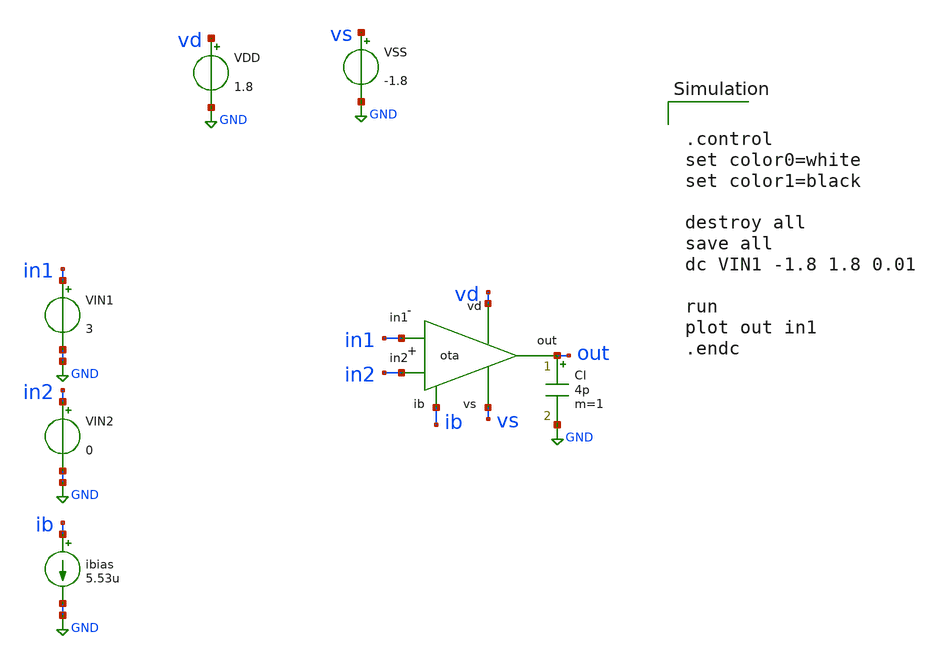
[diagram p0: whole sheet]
** sch_path: amp-op/xschem/ota_tb-dc.sch
* Copyright 2020 Stefan Frederik Schippers
* Licensed under the Apache License, Version 2.0 (the "License");
* you may not use this file except in compliance with the License.
* You may obtain a copy of the License at
* https://www.apache.org/licenses/LICENSE-2.0
* Unless required by applicable law or agreed to in writing, software
* distributed under the License is distributed on an "AS IS" BASIS,
* WITHOUT WARRANTIES OR CONDITIONS OF ANY KIND, either express or implied.
* See the License for the specific language governing permissions and
* limitations under the License.
**.subckt ota_tb-dc
VIN2 in2 GND 0
VIN1 in1 GND 3
ibias ib GND 5.53u
VDD vd GND 1.8
VSS vs GND -1.8
Cl out GND 4p m=1
X1 vd ib out in2 in1 vs ota
**** begin user architecture code


.control
set color0=white
set color1=black

destroy all
save all
dc VIN1 -1.8 1.8 0.01

run
plot out in1
.endc

 .lib $::SKYWATER_MODELS/sky130.lib.spice tt
.include $::SKYWATER_STDCELLS/sky130_fd_sc_hd.spice

**** end user architecture code
**.ends

* expanding   symbol:  /home/hugodg/projects-sky130/temp-sensor/amp-op/xschem/ota.sym # of pins=6
** sym_path: amp-op/xschem/ota.sym
** sch_path: amp-op/xschem/ota.sch
.subckt ota vd ib out in2 in1 vs
*.iopin vd
*.iopin vs
*.iopin ib
*.ipin in1
*.ipin in2
*.opin out
XCC out d sky130_fd_pr__cap_mim_m3_1 W=21 L=21 MF=1 m=1
XM5 ib ib vd vd sky130_fd_pr__pfet_01v8 L=1 W=6 nf=1 ad='int((nf+1)/2) * W/nf * 0.29' as='int((nf+2)/2) * W/nf * 0.29'
+ pd='2*int((nf+1)/2) * (W/nf + 0.29)' ps='2*int((nf+2)/2) * (W/nf + 0.29)' nrd='0.29 / W' nrs='0.29 / W'
+ sa=0 sb=0 sd=0 mult=1 m=1
XM6 b ib vd vd sky130_fd_pr__pfet_01v8 L=1 W=6 nf=1 ad='int((nf+1)/2) * W/nf * 0.29' as='int((nf+2)/2) * W/nf * 0.29'
+ pd='2*int((nf+1)/2) * (W/nf + 0.29)' ps='2*int((nf+2)/2) * (W/nf + 0.29)' nrd='0.29 / W' nrs='0.29 / W'
+ sa=0 sb=0 sd=0 mult=1 m=1
XM8 out ib vd vd sky130_fd_pr__pfet_01v8 L=1 W=30 nf=4 ad='int((nf+1)/2) * W/nf * 0.29' as='int((nf+2)/2) * W/nf * 0.29'
+ pd='2*int((nf+1)/2) * (W/nf + 0.29)' ps='2*int((nf+2)/2) * (W/nf + 0.29)' nrd='0.29 / W' nrs='0.29 / W'
+ sa=0 sb=0 sd=0 mult=1 m=1
XM1 c in1 b b sky130_fd_pr__pfet_01v8 L=1 W=3 nf=1 ad='int((nf+1)/2) * W/nf * 0.29' as='int((nf+2)/2) * W/nf * 0.29'
+ pd='2*int((nf+1)/2) * (W/nf + 0.29)' ps='2*int((nf+2)/2) * (W/nf + 0.29)' nrd='0.29 / W' nrs='0.29 / W'
+ sa=0 sb=0 sd=0 mult=1 m=1
XM2 d in2 b b sky130_fd_pr__pfet_01v8 L=1 W=3 nf=1 ad='int((nf+1)/2) * W/nf * 0.29' as='int((nf+2)/2) * W/nf * 0.29'
+ pd='2*int((nf+1)/2) * (W/nf + 0.29)' ps='2*int((nf+2)/2) * (W/nf + 0.29)' nrd='0.29 / W' nrs='0.29 / W'
+ sa=0 sb=0 sd=0 mult=1 m=1
XM3 c c vs vs sky130_fd_pr__nfet_01v8 L=1 W=1 nf=1 ad='int((nf+1)/2) * W/nf * 0.29' as='int((nf+2)/2) * W/nf * 0.29'
+ pd='2*int((nf+1)/2) * (W/nf + 0.29)' ps='2*int((nf+2)/2) * (W/nf + 0.29)' nrd='0.29 / W' nrs='0.29 / W'
+ sa=0 sb=0 sd=0 mult=1 m=1
XM4 d c vs vs sky130_fd_pr__nfet_01v8 L=1 W=1 nf=1 ad='int((nf+1)/2) * W/nf * 0.29' as='int((nf+2)/2) * W/nf * 0.29'
+ pd='2*int((nf+1)/2) * (W/nf + 0.29)' ps='2*int((nf+2)/2) * (W/nf + 0.29)' nrd='0.29 / W' nrs='0.29 / W'
+ sa=0 sb=0 sd=0 mult=1 m=1
XM7 out d vs vs sky130_fd_pr__nfet_01v8 L=1 W=9 nf=2 ad='int((nf+1)/2) * W/nf * 0.29' as='int((nf+2)/2) * W/nf * 0.29'
+ pd='2*int((nf+1)/2) * (W/nf + 0.29)' ps='2*int((nf+2)/2) * (W/nf + 0.29)' nrd='0.29 / W' nrs='0.29 / W'
+ sa=0 sb=0 sd=0 mult=1 m=1
.ends

.GLOBAL GND
.end
